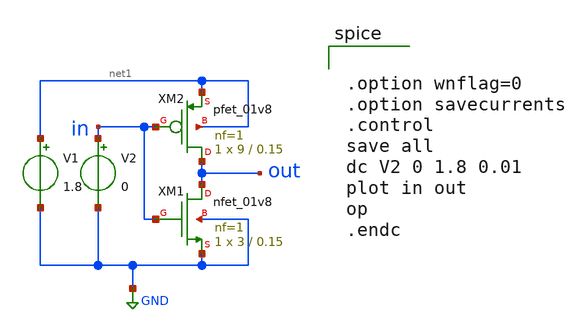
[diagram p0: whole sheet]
** sch_path: inverter.sch
**.subckt inverter
XXM1 out in GND GND sky130_fd_pr__nfet_01v8 L=0.15 W=3 nf=1 ad='int((1 + 1)/2) * 3 / 1 * 0.29' as='int((1 + 2)/2) * 3 / 1 * 0.29'
+ pd='2*int((1 + 1)/2) * (3 / 1 + 0.29)' ps='2*int((1 + 2)/2) * (3 / 1 + 0.29)' nrd='0.29 / 3 ' nrs='0.29 / 3 '
+ sa=0 sb=0 sd=0 mult=1 m=1
XXM2 out in net1 net1 sky130_fd_pr__pfet_01v8 L=0.15 W=9 nf=1 ad='int((1 + 1)/2) * 9 / 1 * 0.29' as='int((1 + 2)/2) * 9 / 1 * 0.29'
+ pd='2*int((1 + 1)/2) * (9 / 1 + 0.29)' ps='2*int((1 + 2)/2) * (9 / 1 + 0.29)' nrd='0.29 / 9 ' nrs='0.29 / 9 '
+ sa=0 sb=0 sd=0 mult=1 m=1
V2 in GND 0
V1 net1 GND 1.8
**** begin user architecture code



.option wnflag=0
.option savecurrents
.control
save all
dc V2 0 1.8 0.01
plot in out
op
.endc


**** end user architecture code
**.ends
.GLOBAL GND
.end
